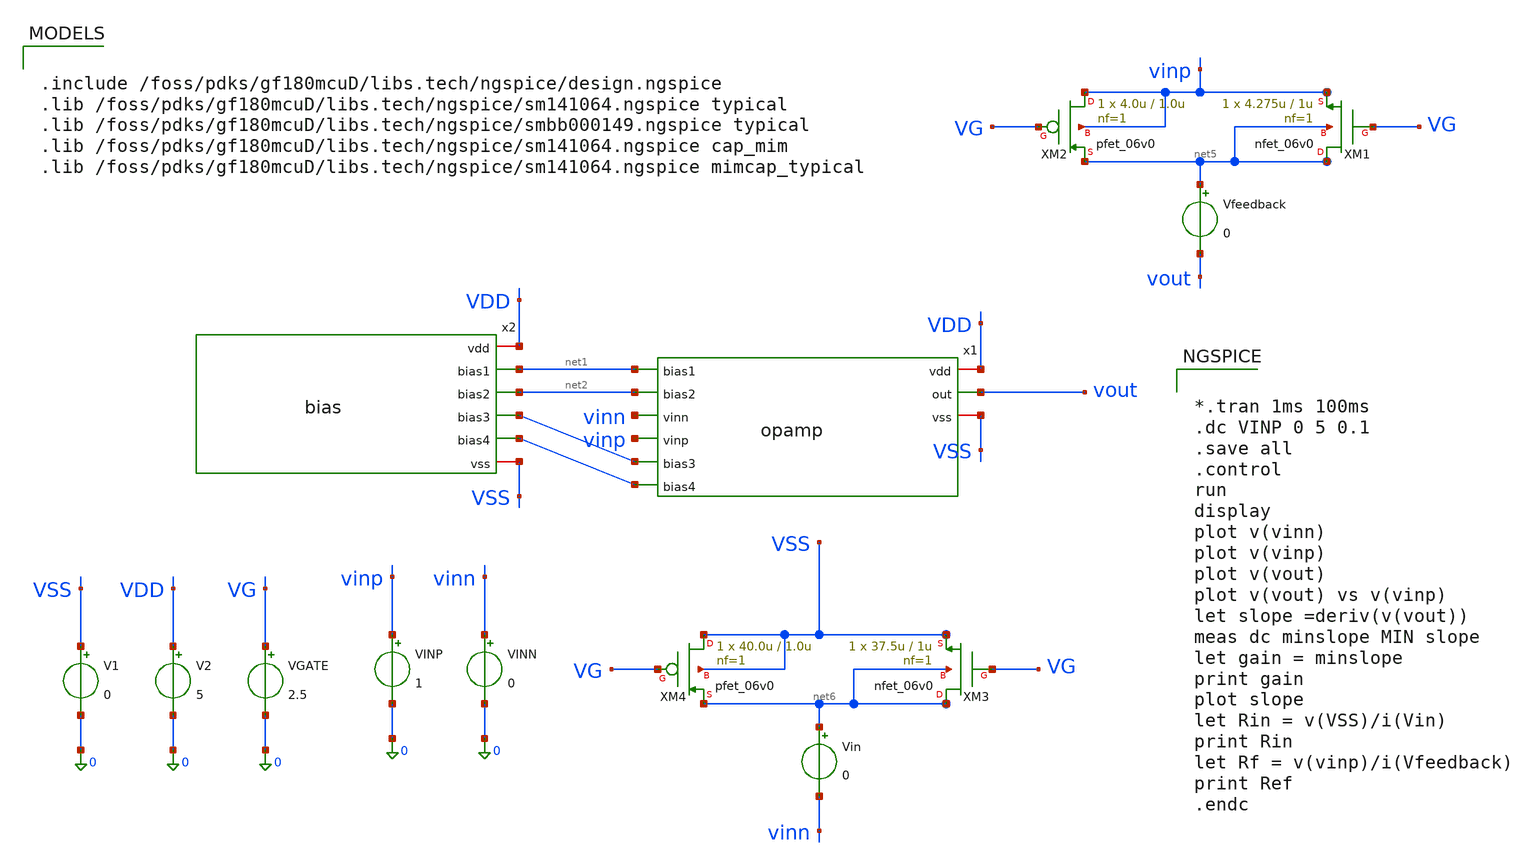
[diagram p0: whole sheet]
** sch_path: activities/opamp3An/OpAmpWFeedback.sch
**.subckt OpAmpWFeedback
x1 VDD net1 net2 vinn vout vinp net4 net3 VSS opamp
x2 VDD net1 net2 net4 net3 VSS bias
V1 VSS 0 0
V2 VDD 0 5
VGATE VG 0 2.5
VINP vinp 0 1
XM1 net5 VG vinp net5 nfet_06v0 L=1u W=4.275u nf=1 ad='int((nf+1)/2) * W/nf * 0.18u' as='int((nf+2)/2) * W/nf * 0.18u'
+ pd='2*int((nf+1)/2) * (W/nf + 0.18u)' ps='2*int((nf+2)/2) * (W/nf + 0.18u)' nrd='0.18u / W' nrs='0.18u / W'
+ sa=0 sb=0 sd=0 m=1
XM2 vinp VG net5 vinp pfet_06v0 L=1.0u W=4.0u nf=1 ad='int((nf+1)/2) * W/nf * 0.18u' as='int((nf+2)/2) * W/nf * 0.18u'
+ pd='2*int((nf+1)/2) * (W/nf + 0.18u)' ps='2*int((nf+2)/2) * (W/nf + 0.18u)' nrd='0.18u / W' nrs='0.18u / W'
+ sa=0 sb=0 sd=0 m=1
XM3 net6 VG VSS net6 nfet_06v0 L=1u W=37.5u nf=1 ad='int((nf+1)/2) * W/nf * 0.18u' as='int((nf+2)/2) * W/nf * 0.18u'
+ pd='2*int((nf+1)/2) * (W/nf + 0.18u)' ps='2*int((nf+2)/2) * (W/nf + 0.18u)' nrd='0.18u / W' nrs='0.18u / W'
+ sa=0 sb=0 sd=0 m=1
XM4 VSS VG net6 VSS pfet_06v0 L=1.0u W=40.0u nf=1 ad='int((nf+1)/2) * W/nf * 0.18u' as='int((nf+2)/2) * W/nf * 0.18u'
+ pd='2*int((nf+1)/2) * (W/nf + 0.18u)' ps='2*int((nf+2)/2) * (W/nf + 0.18u)' nrd='0.18u / W' nrs='0.18u / W'
+ sa=0 sb=0 sd=0 m=1
VINN vinn 0 0
Vfeedback net5 vout 0
Vin net6 vinn 0
**** begin user architecture code


.include /foss/pdks/gf180mcuD/libs.tech/ngspice/design.ngspice
.lib /foss/pdks/gf180mcuD/libs.tech/ngspice/sm141064.ngspice typical
.lib /foss/pdks/gf180mcuD/libs.tech/ngspice/smbb000149.ngspice typical
.lib /foss/pdks/gf180mcuD/libs.tech/ngspice/sm141064.ngspice cap_mim
.lib /foss/pdks/gf180mcuD/libs.tech/ngspice/sm141064.ngspice mimcap_typical




*.tran 1ms 100ms
.dc VINP 0 5 0.1
.save all
.control
run
display
plot v(vinn)
plot v(vinp)
plot v(vout)
plot v(vout) vs v(vinp)
let slope =deriv(v(vout))
meas dc minslope MIN slope
let gain = minslope
print gain
plot slope
let Rin = v(VSS)/i(Vin)
print Rin
let Rf = v(vinp)/i(Vfeedback)
print Ref
.endc


**** end user architecture code
**.ends
.end
